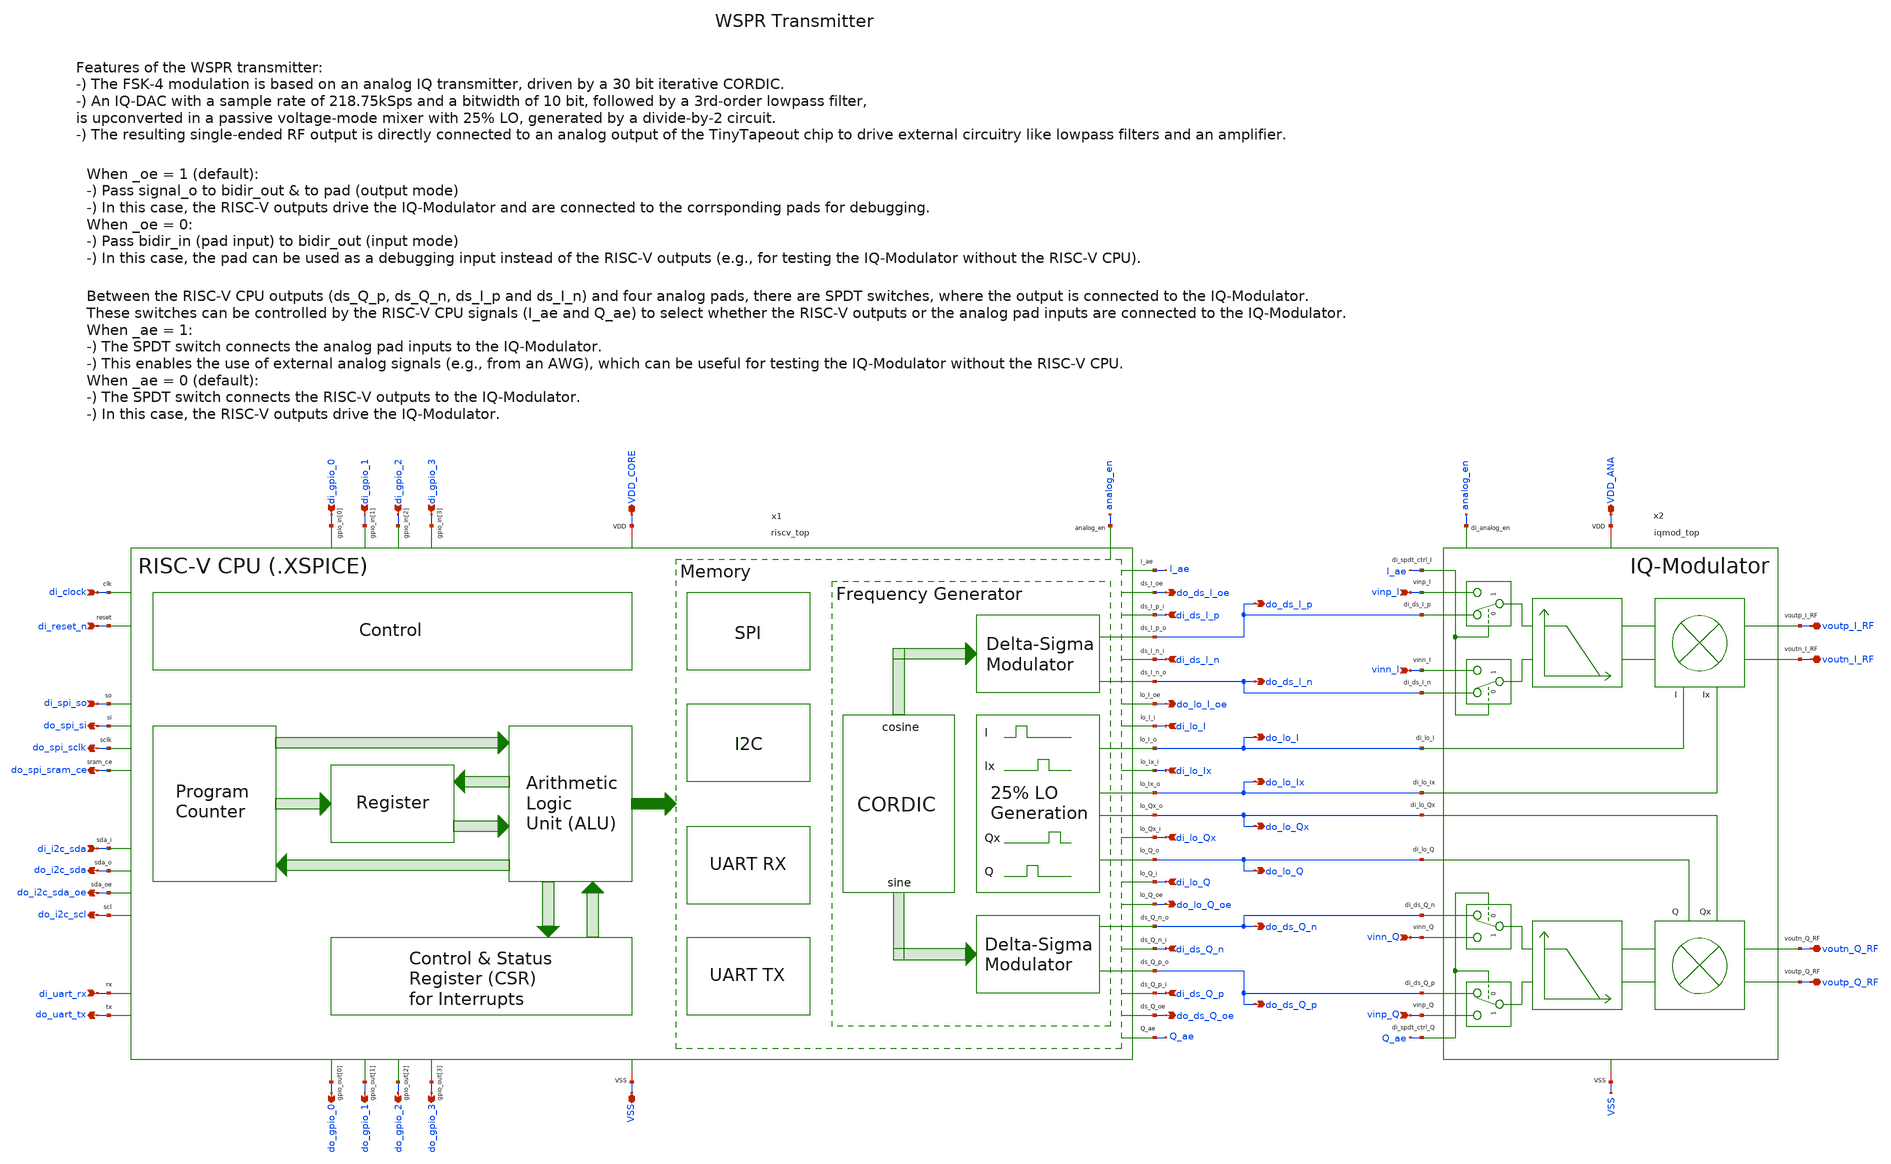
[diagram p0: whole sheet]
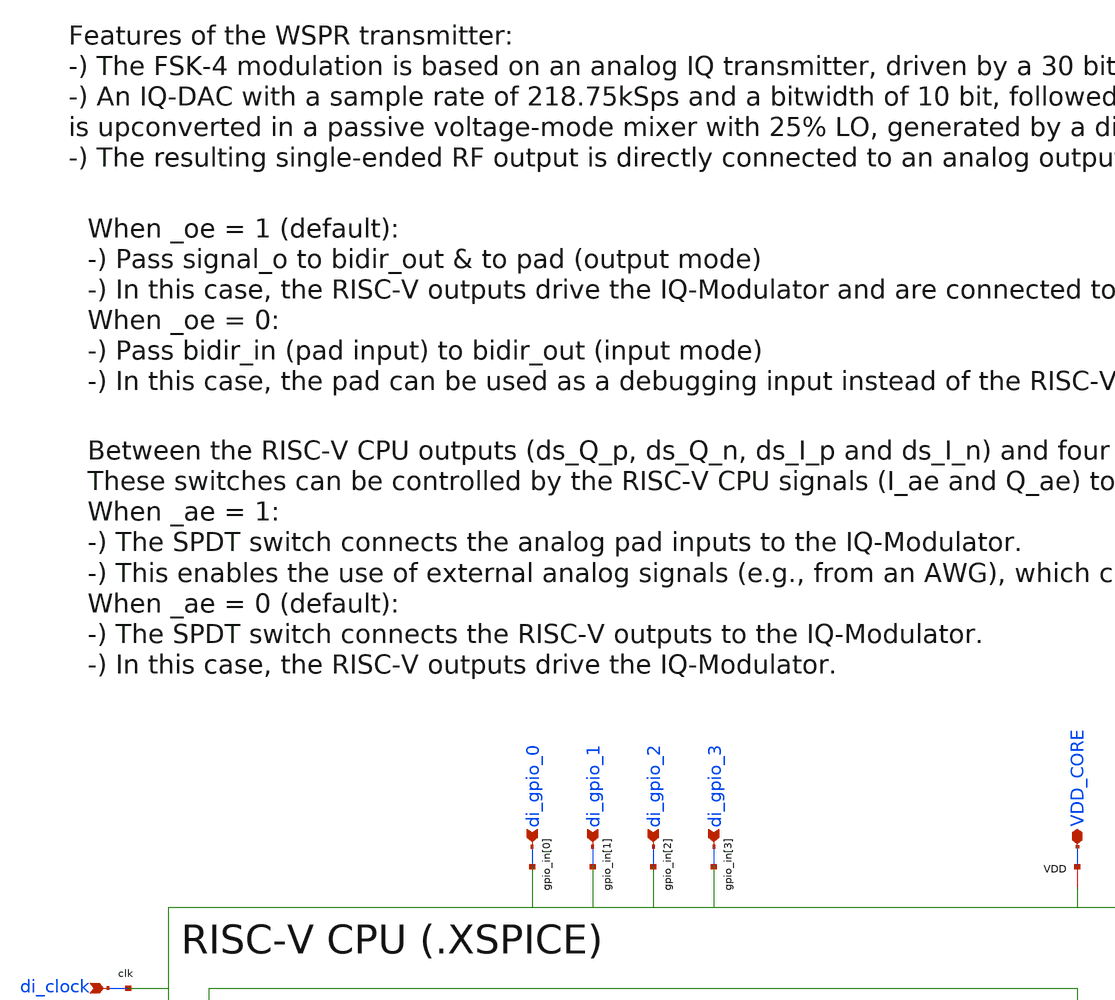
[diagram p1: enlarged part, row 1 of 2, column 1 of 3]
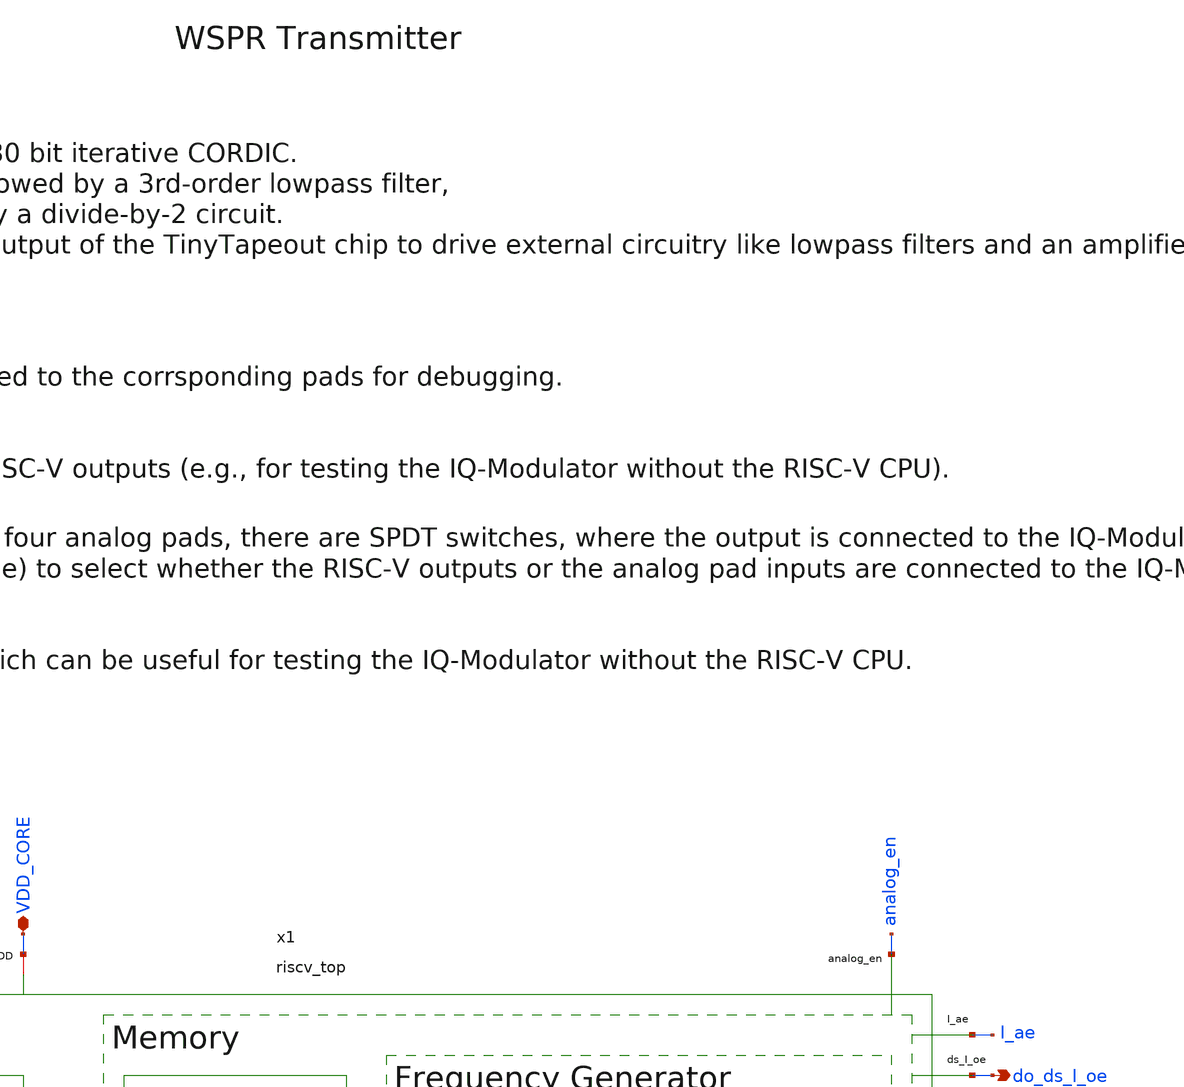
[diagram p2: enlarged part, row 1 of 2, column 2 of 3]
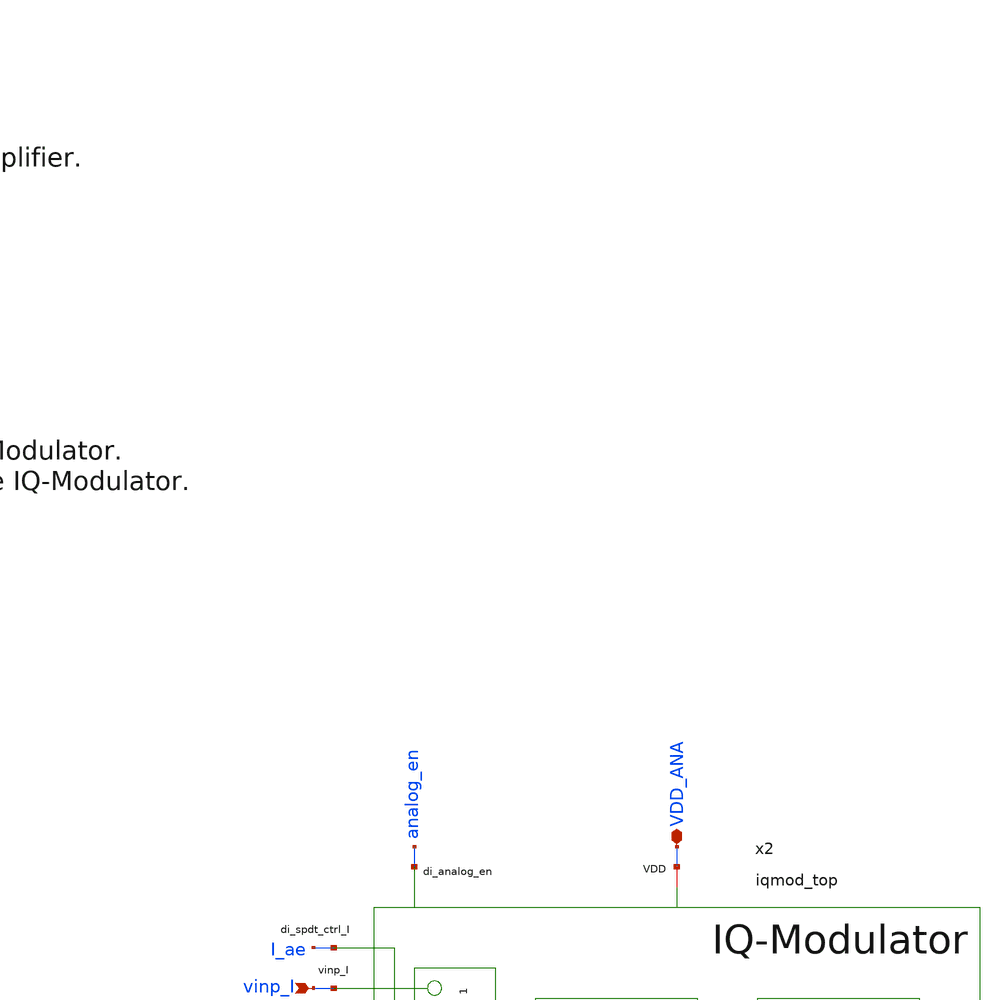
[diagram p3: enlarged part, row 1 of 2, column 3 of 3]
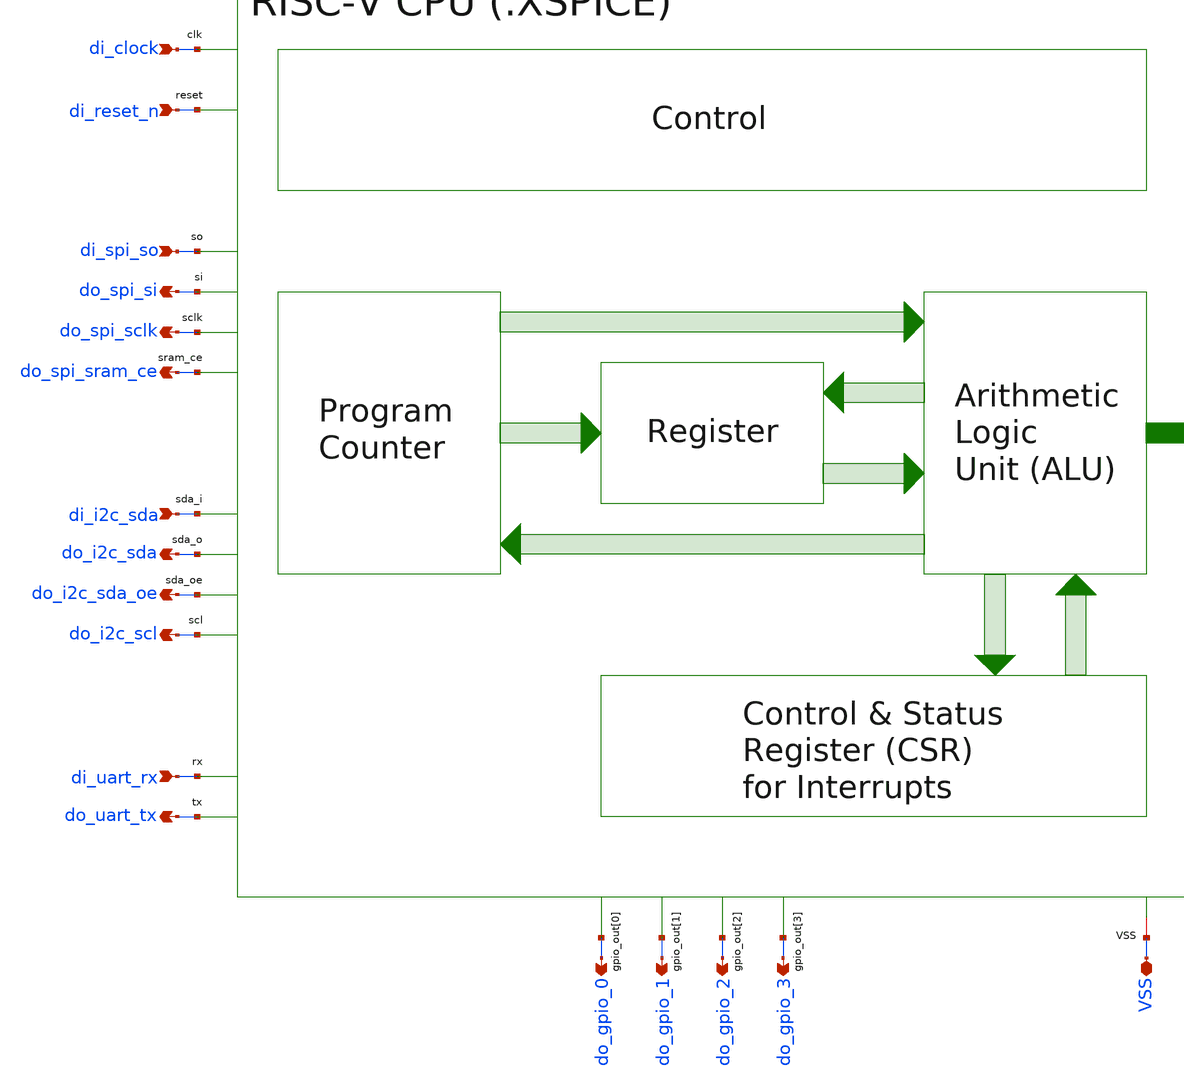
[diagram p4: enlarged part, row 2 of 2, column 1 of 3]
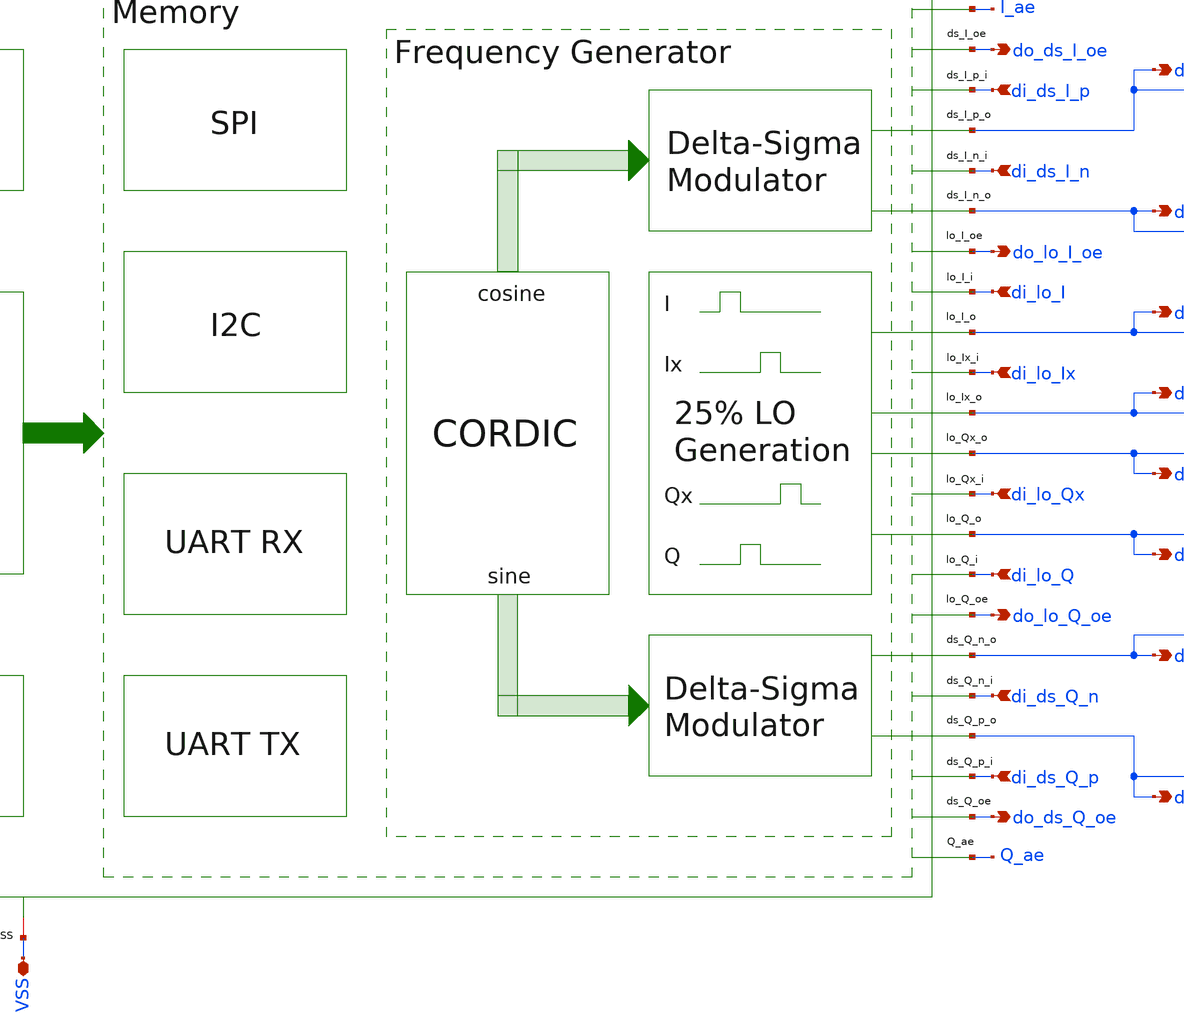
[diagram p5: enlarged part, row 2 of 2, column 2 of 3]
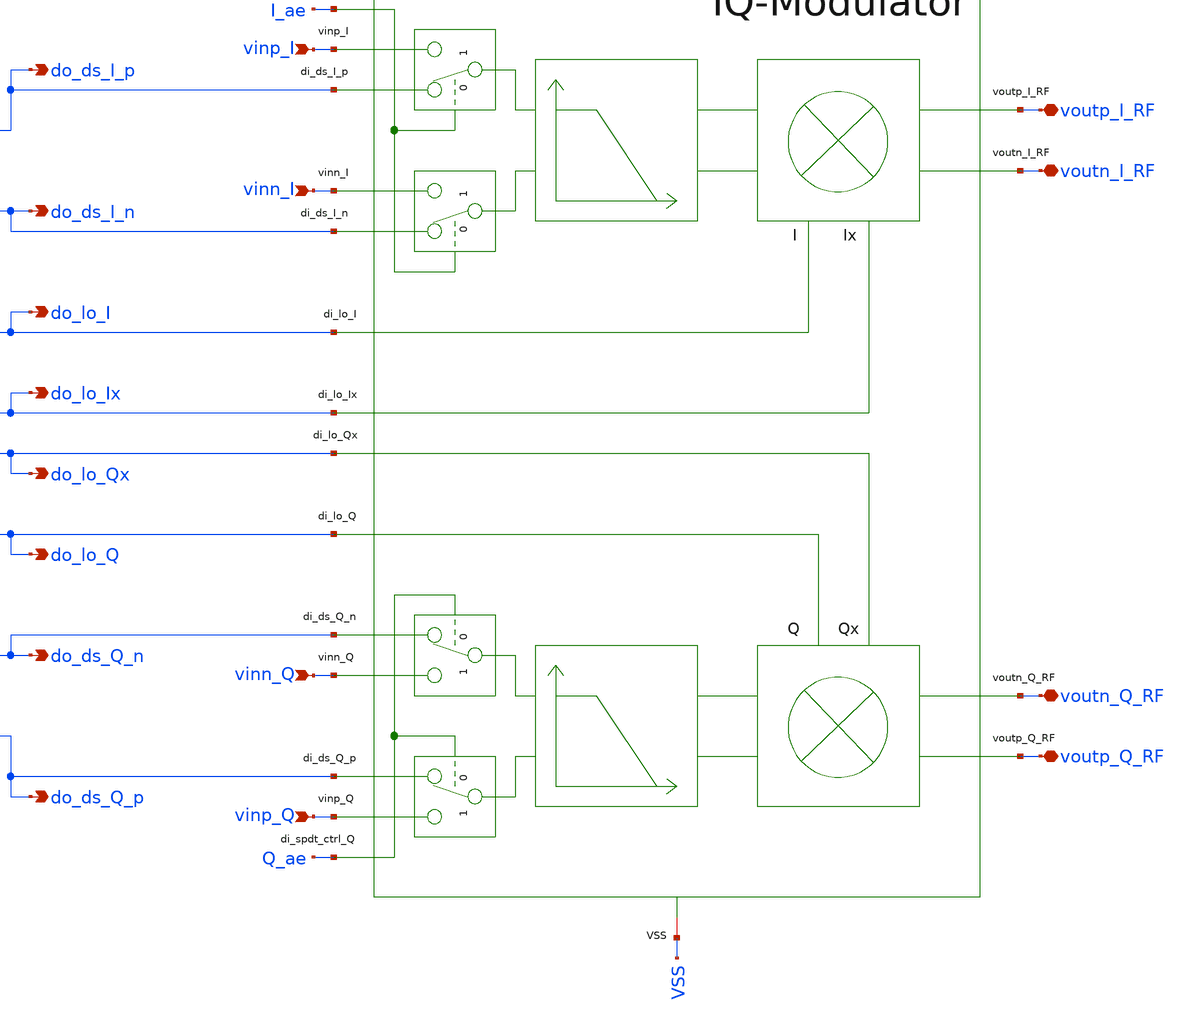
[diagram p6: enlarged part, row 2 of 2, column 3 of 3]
** sch_path: ihp130/schematic/xschem/tinywhisper.sch
**.subckt tinywhisper VDD_CORE VSS di_clock di_reset_n di_spi_so di_i2c_sda voutp_I_RF voutn_I_RF
*+ voutp_Q_RF voutn_Q_RF di_gpio_3 do_gpio_3 di_gpio_2 di_gpio_1 di_gpio_0 do_gpio_2 do_gpio_1 do_gpio_0
*+ di_uart_rx do_uart_tx do_spi_si do_spi_sclk do_spi_sram_ce do_i2c_sda do_i2c_sda_oe do_i2c_scl do_lo_I_oe
*+ do_lo_Q_oe do_ds_Q_oe do_ds_I_oe vinp_I vinn_I vinp_Q vinn_Q di_ds_I_p di_ds_I_n di_lo_I di_lo_Ix di_lo_Qx
*+ di_lo_Q do_ds_I_n do_ds_I_p do_ds_Q_p do_ds_Q_n do_lo_I do_lo_Ix do_lo_Qx do_lo_Q di_ds_Q_n di_ds_Q_p
*+ VDD_ANA
*.iopin VDD_CORE
*.iopin VSS
*.ipin di_clock
*.ipin di_reset_n
*.ipin di_spi_so
*.ipin di_i2c_sda
*.iopin voutp_I_RF
*.iopin voutn_I_RF
*.iopin voutp_Q_RF
*.iopin voutn_Q_RF
*.ipin di_gpio_3
*.opin do_gpio_3
*.ipin di_gpio_2
*.ipin di_gpio_1
*.ipin di_gpio_0
*.opin do_gpio_2
*.opin do_gpio_1
*.opin do_gpio_0
*.ipin di_uart_rx
*.opin do_uart_tx
*.opin do_spi_si
*.opin do_spi_sclk
*.opin do_spi_sram_ce
*.opin do_i2c_sda
*.opin do_i2c_sda_oe
*.opin do_i2c_scl
*.opin do_lo_I_oe
*.opin do_lo_Q_oe
*.opin do_ds_Q_oe
*.opin do_ds_I_oe
*.ipin vinp_I
*.ipin vinn_I
*.ipin vinp_Q
*.ipin vinn_Q
*.ipin di_ds_I_p
*.ipin di_ds_I_n
*.ipin di_lo_I
*.ipin di_lo_Ix
*.ipin di_lo_Qx
*.ipin di_lo_Q
*.opin do_ds_I_n
*.opin do_ds_I_p
*.opin do_ds_Q_p
*.opin do_ds_Q_n
*.opin do_lo_I
*.opin do_lo_Ix
*.opin do_lo_Qx
*.opin do_lo_Q
*.ipin di_ds_Q_n
*.ipin di_ds_Q_p
*.iopin VDD_ANA
x1 VDD_CORE VSS I_ae Q_ae di_clock di_ds_I_n do_ds_I_n do_ds_I_oe di_ds_I_p do_ds_I_p di_ds_Q_n
+ do_ds_Q_n do_ds_Q_oe di_ds_Q_p do_ds_Q_p di_lo_I do_lo_I do_lo_I_oe di_lo_Ix do_lo_Ix di_lo_Q do_lo_Q
+ do_lo_Q_oe di_lo_Qx do_lo_Qx di_reset_n di_uart_rx do_i2c_scl do_spi_sclk di_i2c_sda do_i2c_sda do_i2c_sda_oe
+ do_spi_si di_spi_so do_spi_sram_ce do_uart_tx di_gpio_0 di_gpio_1 di_gpio_2 di_gpio_3 do_gpio_0 do_gpio_1
+ do_gpio_2 do_gpio_3 analog_en riscv_top
x2 do_ds_I_p I_ae do_ds_I_n do_ds_Q_n Q_ae do_ds_Q_p vinp_Q vinn_Q do_lo_I do_lo_Ix voutp_I_RF
+ vinp_I vinn_I do_lo_Q do_lo_Qx voutn_I_RF voutp_Q_RF voutn_Q_RF VDD_ANA VSS analog_en iqmod_top
**.ends
.end
